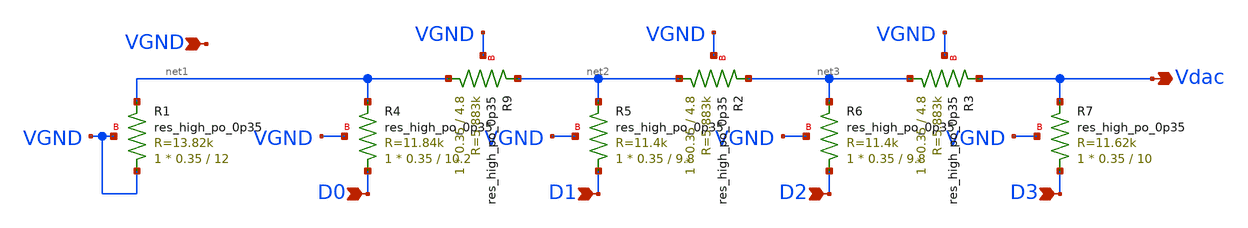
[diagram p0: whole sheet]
** sch_path: xschem/subckts/DAC.sch
**.subckt DAC Vdac D0 D1 D2 D3 VGND
*.opin Vdac
*.ipin D0
*.ipin D1
*.ipin D2
*.ipin D3
*.ipin VGND
XR1 VGND net1 VGND sky130_fd_pr__res_high_po_0p35 L=12 mult=1 m=1
XR9 net1 net2 VGND sky130_fd_pr__res_high_po_0p35 L=4.8 mult=1 m=1
XR2 net2 net3 VGND sky130_fd_pr__res_high_po_0p35 L=4.8 mult=1 m=1
XR3 net3 Vdac VGND sky130_fd_pr__res_high_po_0p35 L=4.8 mult=1 m=1
XR4 D0 net1 VGND sky130_fd_pr__res_high_po_0p35 L=10.2 mult=1 m=1
XR5 D1 net2 VGND sky130_fd_pr__res_high_po_0p35 L=9.8 mult=1 m=1
XR6 D2 net3 VGND sky130_fd_pr__res_high_po_0p35 L=9.8 mult=1 m=1
XR7 D3 Vdac VGND sky130_fd_pr__res_high_po_0p35 L=10 mult=1 m=1
**.ends
.end
